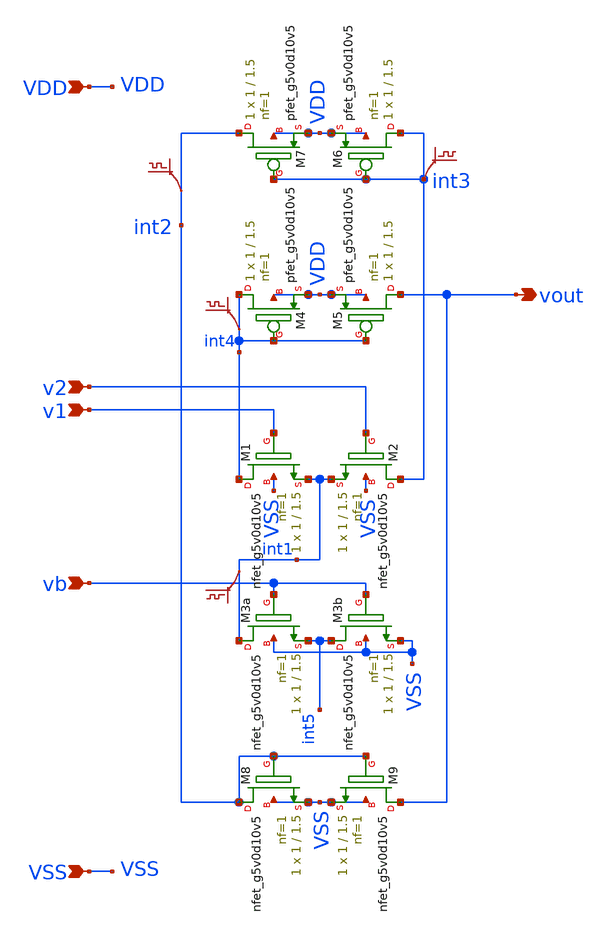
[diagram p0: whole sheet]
** sch_path: xschem/diffamp_nmos.sch
**.subckt diffamp_nmos v1 v2 VSS VDD vb vout
*.ipin v1
*.ipin v2
*.ipin VSS
*.ipin VDD
*.ipin vb
*.opin vout
XM1 int4 v1 int1 VSS sky130_fd_pr__nfet_g5v0d10v5 L=1.5 W=1 nf=1 ad='int((nf+1)/2) * W/nf * 0.29' as='int((nf+2)/2) * W/nf * 0.29'
+ pd='2*int((nf+1)/2) * (W/nf + 0.29)' ps='2*int((nf+2)/2) * (W/nf + 0.29)' nrd='0.29 / W' nrs='0.29 / W'
+ sa=0 sb=0 sd=0 mult=1 m=1
XM2 int3 v2 int1 VSS sky130_fd_pr__nfet_g5v0d10v5 L=1.5 W=1 nf=1 ad='int((nf+1)/2) * W/nf * 0.29' as='int((nf+2)/2) * W/nf * 0.29'
+ pd='2*int((nf+1)/2) * (W/nf + 0.29)' ps='2*int((nf+2)/2) * (W/nf + 0.29)' nrd='0.29 / W' nrs='0.29 / W'
+ sa=0 sb=0 sd=0 mult=1 m=1
XM3a int1 vb int5 VSS sky130_fd_pr__nfet_g5v0d10v5 L=1.5 W=1 nf=1 ad='int((nf+1)/2) * W/nf * 0.29' as='int((nf+2)/2) * W/nf * 0.29'
+ pd='2*int((nf+1)/2) * (W/nf + 0.29)' ps='2*int((nf+2)/2) * (W/nf + 0.29)' nrd='0.29 / W' nrs='0.29 / W'
+ sa=0 sb=0 sd=0 mult=1 m=1
XM4 int4 int4 VDD VDD sky130_fd_pr__pfet_g5v0d10v5 L=1.5 W=1 nf=1 ad='int((nf+1)/2) * W/nf * 0.29' as='int((nf+2)/2) * W/nf * 0.29'
+ pd='2*int((nf+1)/2) * (W/nf + 0.29)' ps='2*int((nf+2)/2) * (W/nf + 0.29)' nrd='0.29 / W' nrs='0.29 / W'
+ sa=0 sb=0 sd=0 mult=1 m=1
XM5 vout int4 VDD VDD sky130_fd_pr__pfet_g5v0d10v5 L=1.5 W=1 nf=1 ad='int((nf+1)/2) * W/nf * 0.29' as='int((nf+2)/2) * W/nf * 0.29'
+ pd='2*int((nf+1)/2) * (W/nf + 0.29)' ps='2*int((nf+2)/2) * (W/nf + 0.29)' nrd='0.29 / W' nrs='0.29 / W'
+ sa=0 sb=0 sd=0 mult=1 m=1
XM6 int3 int3 VDD VDD sky130_fd_pr__pfet_g5v0d10v5 L=1.5 W=1 nf=1 ad='int((nf+1)/2) * W/nf * 0.29' as='int((nf+2)/2) * W/nf * 0.29'
+ pd='2*int((nf+1)/2) * (W/nf + 0.29)' ps='2*int((nf+2)/2) * (W/nf + 0.29)' nrd='0.29 / W' nrs='0.29 / W'
+ sa=0 sb=0 sd=0 mult=1 m=1
XM7 int2 int3 VDD VDD sky130_fd_pr__pfet_g5v0d10v5 L=1.5 W=1 nf=1 ad='int((nf+1)/2) * W/nf * 0.29' as='int((nf+2)/2) * W/nf * 0.29'
+ pd='2*int((nf+1)/2) * (W/nf + 0.29)' ps='2*int((nf+2)/2) * (W/nf + 0.29)' nrd='0.29 / W' nrs='0.29 / W'
+ sa=0 sb=0 sd=0 mult=1 m=1
XM8 int2 int2 VSS VSS sky130_fd_pr__nfet_g5v0d10v5 L=1.5 W=1 nf=1 ad='int((nf+1)/2) * W/nf * 0.29' as='int((nf+2)/2) * W/nf * 0.29'
+ pd='2*int((nf+1)/2) * (W/nf + 0.29)' ps='2*int((nf+2)/2) * (W/nf + 0.29)' nrd='0.29 / W' nrs='0.29 / W'
+ sa=0 sb=0 sd=0 mult=1 m=1
XM9 vout int2 VSS VSS sky130_fd_pr__nfet_g5v0d10v5 L=1.5 W=1 nf=1 ad='int((nf+1)/2) * W/nf * 0.29' as='int((nf+2)/2) * W/nf * 0.29'
+ pd='2*int((nf+1)/2) * (W/nf + 0.29)' ps='2*int((nf+2)/2) * (W/nf + 0.29)' nrd='0.29 / W' nrs='0.29 / W'
+ sa=0 sb=0 sd=0 mult=1 m=1
XM3b int5 vb VSS VSS sky130_fd_pr__nfet_g5v0d10v5 L=1.5 W=1 nf=1 ad='int((nf+1)/2) * W/nf * 0.29' as='int((nf+2)/2) * W/nf * 0.29'
+ pd='2*int((nf+1)/2) * (W/nf + 0.29)' ps='2*int((nf+2)/2) * (W/nf + 0.29)' nrd='0.29 / W' nrs='0.29 / W'
+ sa=0 sb=0 sd=0 mult=1 m=1
.save v(int1)
.save v(int2)
.save v(int3)
.save v(int4)
**.ends
.end
